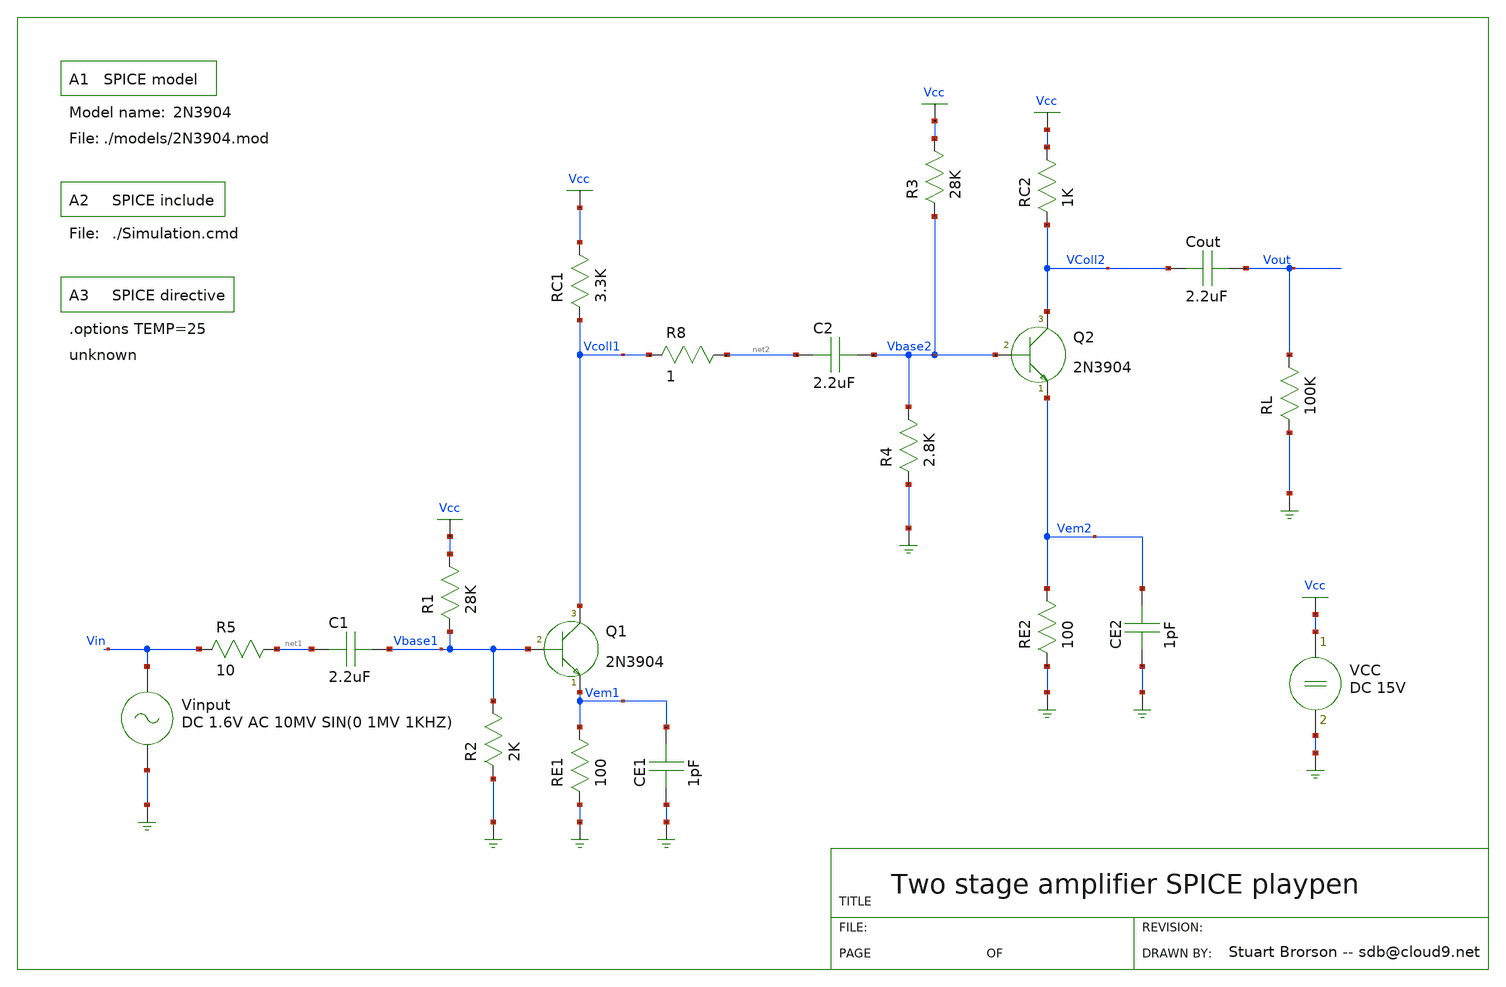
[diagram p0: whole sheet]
** sch_path: xschem_library/gschem_import/TwoStageAmp.sch
**.subckt TwoStageAmp
Q1 Vcoll1 Vbase1 Vem1
R5 Vin net1 10
R1 Vbase1 Vcc 28K
R2 GND Vbase1 2K
RE1 GND Vem1 100
RC2 VColl2 Vcc 1K
RL GND Vout 100K
Cout VColl2 Vout 2.2uF
CE1 GND Vem1 1pF
Vinput Vin GND DC 1.6V AC 10MV SIN(0 1MV 1KHZ)
VCC Vcc GND DC 15V
.include ./models/2N3904.mod
.include ./Simulation.cmd
.options TEMP=25
C1 net1 Vbase1 2.2uF
Q2 VColl2 Vbase2 Vem2
RC1 Vcoll1 Vcc 3.3K
RE2 GND Vem2 100
CE2 GND Vem2 1pF
R8 Vcoll1 net2 1
R3 Vbase2 Vcc 28K
R4 GND Vbase2 2.8K
C2 net2 Vbase2 2.2uF
**.ends
.end
